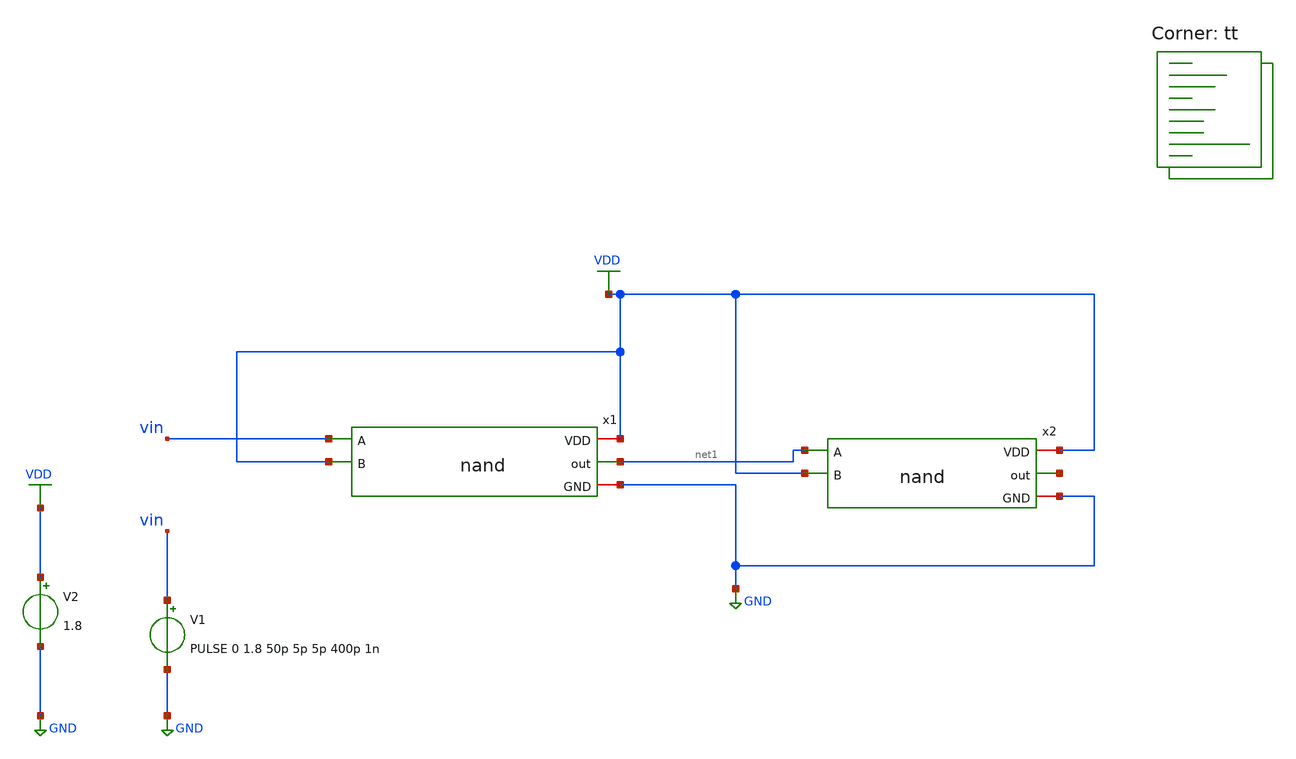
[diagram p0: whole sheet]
** sch_path: assignments/assignment5/assign1a.sch
**.subckt assign1a
x1 VDD vin net1 VDD GND nand
x2 VDD net1 net2 VDD GND nand
V2 VDD GND 1.8
V1 vin GND PULSE 0 1.8 50p 5p 5p 400p 1n
**** begin user architecture code
.lib $::SKYWATER_MODELS/sky130.lib.spice tt


.control
tran 0.1p 1n
meas tran tphl trig v(vin) val=0.9 rise=1 targ v(net1) val=0.9 fall=1
meas tran tplh trig v(vin) val=0.9 fall=1 targ v(net1) val=0.9 rise=1
let tpd = (tphl + tplh) / 2
print tpd

plot v(net1) vin
.endc


**** end user architecture code
**.ends

* expanding   symbol:  nand.sym # of pins=5
** sym_path: assignments/assignment5/nand.sym
** sch_path: assignments/assignment5/nand.sch
.subckt nand VDD A out B GND
*.ipin A
*.opin out
*.iopin VDD
*.iopin GND
*.ipin B
XM1 out A net1 net2 sky130_fd_pr__nfet_01v8 L=0.15 W=1.68 nf=4 ad='int((nf+1)/2) * W/nf * 0.29' as='int((nf+2)/2) * W/nf * 0.29'
+ pd='2*int((nf+1)/2) * (W/nf + 0.29)' ps='2*int((nf+2)/2) * (W/nf + 0.29)' nrd='0.29 / W' nrs='0.29 / W'
+ sa=0 sb=0 sd=0 mult=1 m=1
XM2 out A VDD net3 sky130_fd_pr__pfet_01v8 L=0.15 W=1.68 nf=4 ad='int((nf+1)/2) * W/nf * 0.29' as='int((nf+2)/2) * W/nf * 0.29'
+ pd='2*int((nf+1)/2) * (W/nf + 0.29)' ps='2*int((nf+2)/2) * (W/nf + 0.29)' nrd='0.29 / W' nrs='0.29 / W'
+ sa=0 sb=0 sd=0 mult=1 m=1
XM3 net1 B GND net4 sky130_fd_pr__nfet_01v8 L=0.15 W=1.68 nf=4 ad='int((nf+1)/2) * W/nf * 0.29' as='int((nf+2)/2) * W/nf * 0.29'
+ pd='2*int((nf+1)/2) * (W/nf + 0.29)' ps='2*int((nf+2)/2) * (W/nf + 0.29)' nrd='0.29 / W' nrs='0.29 / W'
+ sa=0 sb=0 sd=0 mult=1 m=1
XM4 out B VDD net5 sky130_fd_pr__pfet_01v8 L=0.15 W=1.68 nf=4 ad='int((nf+1)/2) * W/nf * 0.29' as='int((nf+2)/2) * W/nf * 0.29'
+ pd='2*int((nf+1)/2) * (W/nf + 0.29)' ps='2*int((nf+2)/2) * (W/nf + 0.29)' nrd='0.29 / W' nrs='0.29 / W'
+ sa=0 sb=0 sd=0 mult=1 m=1
.ends

.GLOBAL VDD
.GLOBAL GND
.end
